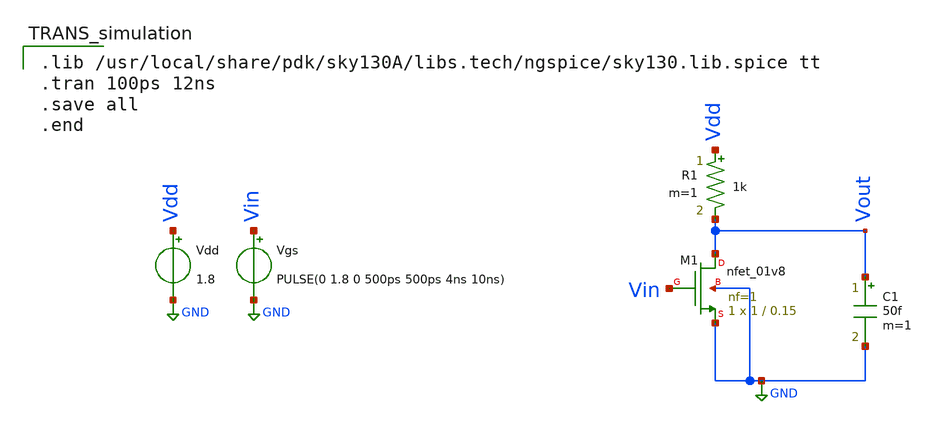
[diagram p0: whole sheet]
** sch_path: Design-and-analysis-of-CMOS-ineverter/XSCHEM FILES/NMOSs0w1.sch
**.subckt NMOSs0w1
XM1 Vout Vin GND GND sky130_fd_pr__nfet_01v8 L=0.15 W=1 nf=1 ad='int((nf+1)/2) * W/nf * 0.29' as='int((nf+2)/2) * W/nf * 0.29'
+ pd='2*int((nf+1)/2) * (W/nf + 0.29)' ps='2*int((nf+2)/2) * (W/nf + 0.29)' nrd='0.29 / W' nrs='0.29 / W'
+ sa=0 sb=0 sd=0 mult=1 m=1
R1 Vdd Vout 1k m=1
C1 Vout GND 50f m=1
Vgs Vin GND PULSE(0 1.8 0 500ps 500ps 4ns 10ns)
Vdd Vdd GND 1.8
**** begin user architecture code

.lib /usr/local/share/pdk/sky130A/libs.tech/ngspice/sky130.lib.spice tt
.tran 100ps 12ns
.save all
.end

**** end user architecture code
**.ends
.GLOBAL GND
.end
